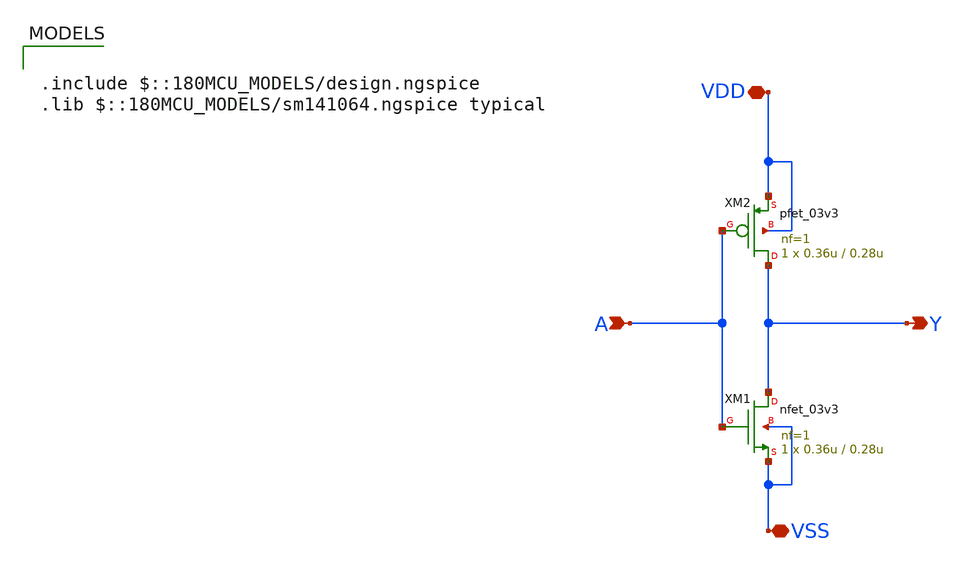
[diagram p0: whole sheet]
** sch_path: member_project/ice458/dynamic_comparator/xschem/inverter.sch
**.subckt inverter Y A VDD VSS
*.opin Y
*.ipin A
*.iopin VDD
*.iopin VSS
XM1 Y A VSS VSS nfet_03v3 L=0.28u W=0.36u nf=1 ad='int((nf+1)/2) * W/nf * 0.18u' as='int((nf+2)/2) * W/nf * 0.18u'
+ pd='2*int((nf+1)/2) * (W/nf + 0.18u)' ps='2*int((nf+2)/2) * (W/nf + 0.18u)' nrd='0.18u / W' nrs='0.18u / W'
+ sa=0 sb=0 sd=0 m=1
XM2 Y A VDD VDD pfet_03v3 L=0.28u W=0.36u nf=1 ad='int((nf+1)/2) * W/nf * 0.18u' as='int((nf+2)/2) * W/nf * 0.18u'
+ pd='2*int((nf+1)/2) * (W/nf + 0.18u)' ps='2*int((nf+2)/2) * (W/nf + 0.18u)' nrd='0.18u / W' nrs='0.18u / W'
+ sa=0 sb=0 sd=0 m=1
**** begin user architecture code

.include $::180MCU_MODELS/design.ngspice
.lib $::180MCU_MODELS/sm141064.ngspice typical

**** end user architecture code
**.ends
.end
